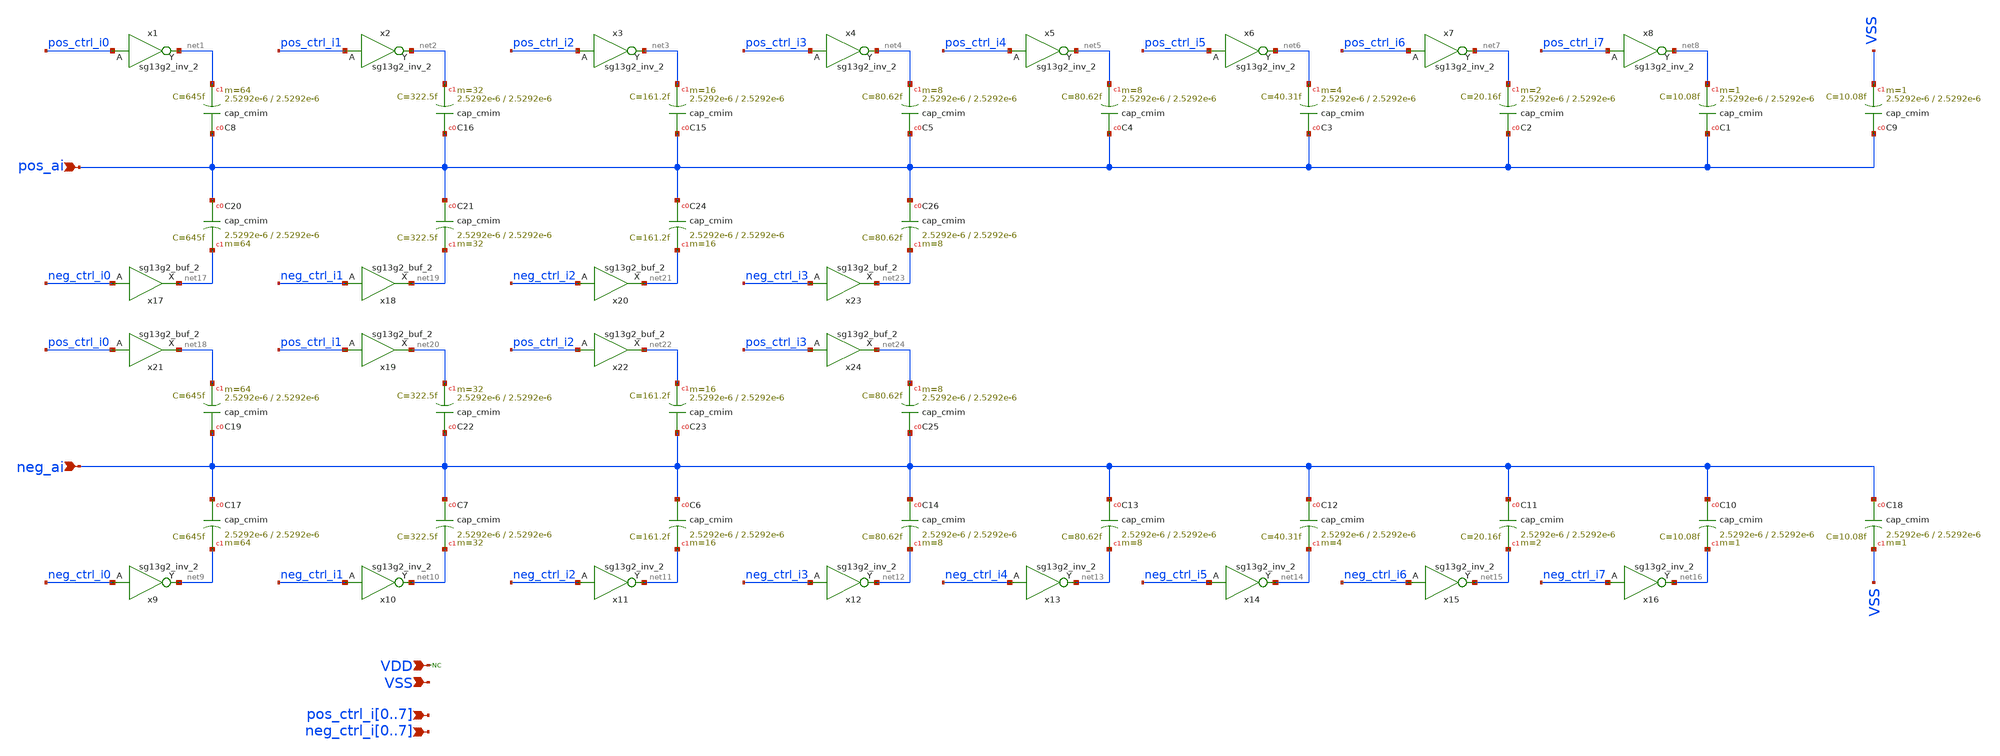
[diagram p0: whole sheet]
** sch_path: designs/cdac_diff/cdac.sch
* IHP-GmbH/IHP-Open-PDK/ihp-sg13g2/libs.tech/xschem/sg13g2_stdcells/sg13g2_inv_2.sch:
* Copyright 2023 IHP PDK Authors
* Licensed under the Apache License, Version 2.0 (the "License");
**.subckt cdac pos_ai VSS VDD neg_ai
*+ pos_ctrl_i0,pos_ctrl_i1,pos_ctrl_i2,pos_ctrl_i3,pos_ctrl_i4,pos_ctrl_i5,pos_ctrl_i6,pos_ctrl_i7 neg_ctrl_i0,neg_ctrl_i1,neg_ctrl_i2,neg_ctrl_i3,neg_ctrl_i4,neg_ctrl_i5,neg_ctrl_i6,neg_ctrl_i7
*.ipin pos_ai
*.ipin VSS
*.ipin VDD
*.ipin neg_ai
*.ipin
*+ pos_ctrl_i0,pos_ctrl_i1,pos_ctrl_i2,pos_ctrl_i3,pos_ctrl_i4,pos_ctrl_i5,pos_ctrl_i6,pos_ctrl_i7
*.ipin
*+ neg_ctrl_i0,neg_ctrl_i1,neg_ctrl_i2,neg_ctrl_i3,neg_ctrl_i4,neg_ctrl_i5,neg_ctrl_i6,neg_ctrl_i7
x1 net1 pos_ctrl_i0 VDD VSS sg13g2_inv_2
x2 net2 pos_ctrl_i1 VDD VSS sg13g2_inv_2
x3 net3 pos_ctrl_i2 VDD VSS sg13g2_inv_2
x4 net4 pos_ctrl_i3 VDD VSS sg13g2_inv_2
x5 net5 pos_ctrl_i4 VDD VSS sg13g2_inv_2
x6 net6 pos_ctrl_i5 VDD VSS sg13g2_inv_2
x7 net7 pos_ctrl_i6 VDD VSS sg13g2_inv_2
x8 net8 pos_ctrl_i7 VDD VSS sg13g2_inv_2
XC1 pos_ai net8 cap_cmim w=2.5292e-6 l=2.5292e-6 m=1 mm_ok=1
XC2 pos_ai net7 cap_cmim w=2.5292e-6 l=2.5292e-6 m=2 mm_ok=1
XC3 pos_ai net6 cap_cmim w=2.5292e-6 l=2.5292e-6 m=4 mm_ok=1
XC4 pos_ai net5 cap_cmim w=2.5292e-6 l=2.5292e-6 m=8 mm_ok=1
XC9 pos_ai VSS cap_cmim w=2.5292e-6 l=2.5292e-6 m=1 mm_ok=1
x9 net9 neg_ctrl_i0 VDD VSS sg13g2_inv_2
x10 net10 neg_ctrl_i1 VDD VSS sg13g2_inv_2
x11 net11 neg_ctrl_i2 VDD VSS sg13g2_inv_2
x12 net12 neg_ctrl_i3 VDD VSS sg13g2_inv_2
x13 net13 neg_ctrl_i4 VDD VSS sg13g2_inv_2
x14 net14 neg_ctrl_i5 VDD VSS sg13g2_inv_2
x15 net15 neg_ctrl_i6 VDD VSS sg13g2_inv_2
x16 net16 neg_ctrl_i7 VDD VSS sg13g2_inv_2
XC10 neg_ai net16 cap_cmim w=2.5292e-6 l=2.5292e-6 m=1 mm_ok=1
XC11 neg_ai net15 cap_cmim w=2.5292e-6 l=2.5292e-6 m=2 mm_ok=1
XC12 neg_ai net14 cap_cmim w=2.5292e-6 l=2.5292e-6 m=4 mm_ok=1
XC13 neg_ai net13 cap_cmim w=2.5292e-6 l=2.5292e-6 m=8 mm_ok=1
XC18 neg_ai VSS cap_cmim w=2.5292e-6 l=2.5292e-6 m=1 mm_ok=1
XC8 pos_ai net1 cap_cmim w=2.5292e-6 l=2.5292e-6 m=64 mm_ok=1
XC17 neg_ai net9 cap_cmim w=2.5292e-6 l=2.5292e-6 m=64 mm_ok=1
XC19 neg_ai net18 cap_cmim w=2.5292e-6 l=2.5292e-6 m=64 mm_ok=1
XC20 pos_ai net17 cap_cmim w=2.5292e-6 l=2.5292e-6 m=64 mm_ok=1
XC7 neg_ai net10 cap_cmim w=2.5292e-6 l=2.5292e-6 m=32 mm_ok=1
XC16 pos_ai net2 cap_cmim w=2.5292e-6 l=2.5292e-6 m=32 mm_ok=1
XC21 pos_ai net19 cap_cmim w=2.5292e-6 l=2.5292e-6 m=32 mm_ok=1
XC22 neg_ai net20 cap_cmim w=2.5292e-6 l=2.5292e-6 m=32 mm_ok=1
XC23 neg_ai net22 cap_cmim w=2.5292e-6 l=2.5292e-6 m=16 mm_ok=1
XC24 pos_ai net21 cap_cmim w=2.5292e-6 l=2.5292e-6 m=16 mm_ok=1
XC6 neg_ai net11 cap_cmim w=2.5292e-6 l=2.5292e-6 m=16 mm_ok=1
XC15 pos_ai net3 cap_cmim w=2.5292e-6 l=2.5292e-6 m=16 mm_ok=1
XC25 neg_ai net24 cap_cmim w=2.5292e-6 l=2.5292e-6 m=8 mm_ok=1
XC26 pos_ai net23 cap_cmim w=2.5292e-6 l=2.5292e-6 m=8 mm_ok=1
XC5 pos_ai net4 cap_cmim w=2.5292e-6 l=2.5292e-6 m=8 mm_ok=1
XC14 neg_ai net12 cap_cmim w=2.5292e-6 l=2.5292e-6 m=8 mm_ok=1
* noconn VDD
x17 net17 neg_ctrl_i0 VDD VSS sg13g2_buf_2
x21 net18 pos_ctrl_i0 VDD VSS sg13g2_buf_2
x18 net19 neg_ctrl_i1 VDD VSS sg13g2_buf_2
x19 net20 pos_ctrl_i1 VDD VSS sg13g2_buf_2
x20 net21 neg_ctrl_i2 VDD VSS sg13g2_buf_2
x22 net22 pos_ctrl_i2 VDD VSS sg13g2_buf_2
x23 net23 neg_ctrl_i3 VDD VSS sg13g2_buf_2
x24 net24 pos_ctrl_i3 VDD VSS sg13g2_buf_2
**.ends

* expanding   symbol:  sg13g2_stdcells/sg13g2_inv_2.sym # of pins=2
** sym_path: sg13g2_stdcells/sg13g2_inv_2.sym
** sch_path: sg13g2_stdcells/sg13g2_inv_2.sch
.subckt sg13g2_inv_2 Y A VDD VSS
*.opin Y
*.ipin A
*.iopin VDD
*.iopin VSS
XM1 Y A VSS VSS sg13_lv_nmos w=1.48u l=130.00n ng=2 m=1 mm_ok=1
XM2 Y A VDD VDD sg13_lv_pmos w=2.24u l=130.00n ng=2 m=1 mm_ok=1
.ends


* expanding   symbol:  sg13g2_stdcells/sg13g2_buf_2.sym # of pins=2
** sym_path: sg13g2_stdcells/sg13g2_buf_2.sym
** sch_path: sg13g2_stdcells/sg13g2_buf_2.sch
.subckt sg13g2_buf_2 X A VDD VSS
*.ipin A
*.opin X
*.iopin VDD
*.iopin VSS
XM1 net1 A VSS VSS sg13_lv_nmos w=640.00n l=130.00n ng=1 m=1 mm_ok=1
XM2 X net1 VSS VSS sg13_lv_nmos w=1.48u l=130.00n ng=2 m=1 mm_ok=1
XM3 net1 A VDD VDD sg13_lv_pmos w=1.000u l=130.00n ng=1 m=1 mm_ok=1
XM4 X net1 VDD VDD sg13_lv_pmos w=2.24u l=130.00n ng=2 m=1 mm_ok=1
.ends

.end
